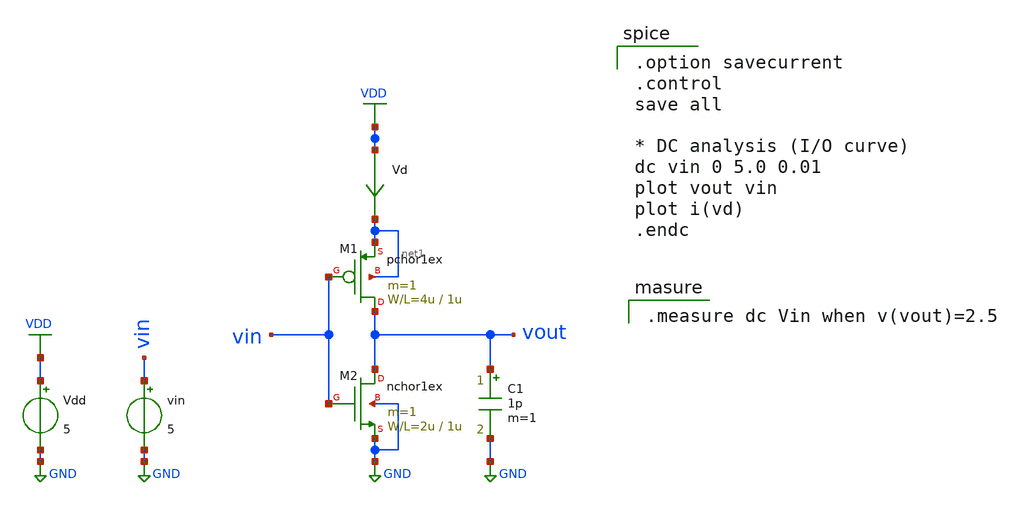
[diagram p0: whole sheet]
** sch_path: member_project/dokunira/inverter_layout/inv_sim.sch
**.subckt inv_sim
C1 vout GND 1p m=1
Vdd VDD GND 5
vin vin GND 5
Vd VDD net1 0
.save i(vd)
M1 vout vin net1 net1 pchor1ex L=1u W=4u m=1
M2 vout vin GND GND nchor1ex L=1u W=2u m=1
**** begin user architecture code
 .include $::LIB/mos.lib
.include $::LIB/passive.lib
.include $::LIB/diode.lib

.option savecurrent
.control
save all

* DC analysis (I/O curve)
dc vin 0 5.0 0.01
plot vout vin
plot i(vd)
.endc



.measure dc Vin when v(vout)=2.5


**** end user architecture code
**.ends
.GLOBAL VDD
.GLOBAL GND
.end
